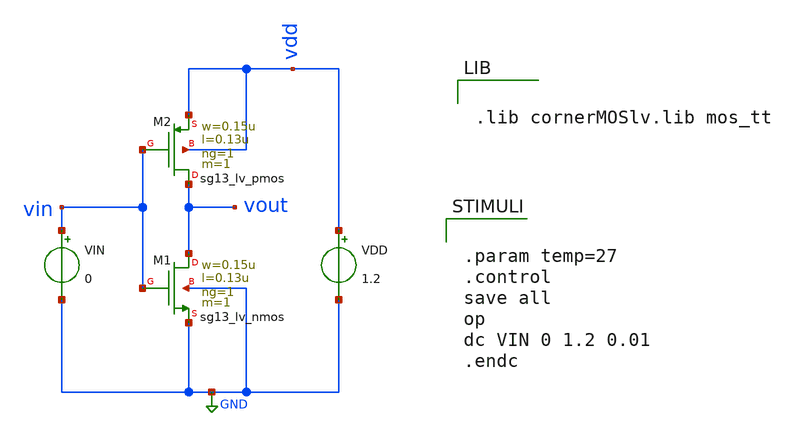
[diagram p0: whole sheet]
** sch_path: BTDay2-Ex/Ex1a_Lecture2.sch
**.subckt Ex1a_Lecture2
XM1 vout vin GND GND sg13_lv_nmos w=0.15u l=0.13u ng=1 m=1 mm_ok=1
XM2 vout vin vdd vdd sg13_lv_pmos w=0.15u l=0.13u ng=1 m=1 mm_ok=1
VIN vin GND 0
VDD vdd GND 1.2
**** begin user architecture code


.lib cornerMOSlv.lib mos_tt




.param temp=27
.control
save all
op
dc VIN 0 1.2 0.01
.endc


**** end user architecture code
**.ends
.GLOBAL GND
.end
